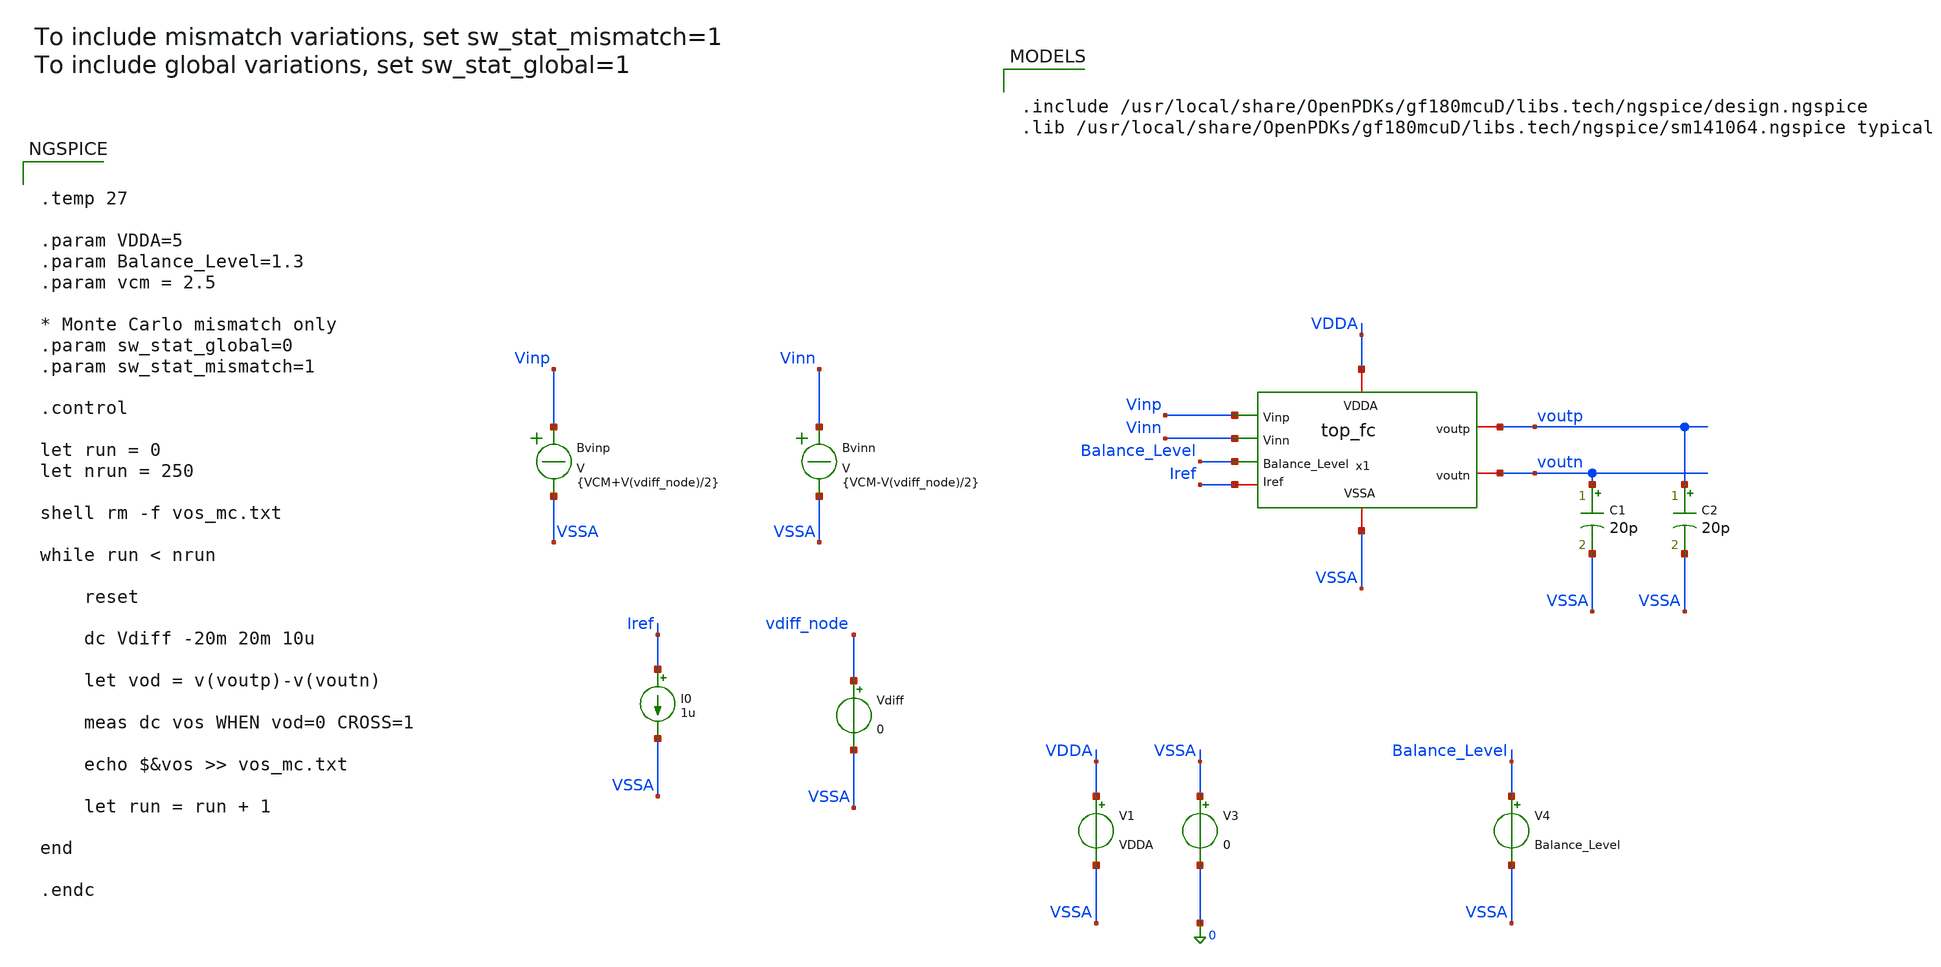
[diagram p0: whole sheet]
** sch_path: Folded_cascode/testbenches/top_fc_offset_tb.sch
**.subckt top_fc_offset_tb
Vdiff vdiff_node VSSA 0
V1 VDDA VSSA VDDA
V3 VSSA 0 0
V4 Balance_Level VSSA Balance_Level
Bvinp Vinp VSSA V = {VCM+V(vdiff_node)/2}
Bvinn Vinn VSSA V = {VCM-V(vdiff_node)/2}
x1 Balance_Level Vinp voutp VDDA voutn Vinn Iref VSSA top_fc
C1 voutn VSSA 20p m=1
C2 voutp VSSA 20p m=1
I0 Iref VSSA 1u
**** begin user architecture code

.include /usr/local/share/OpenPDKs/gf180mcuD/libs.tech/ngspice/design.ngspice
.lib /usr/local/share/OpenPDKs/gf180mcuD/libs.tech/ngspice/sm141064.ngspice typical



.temp 27

.param VDDA=5
.param Balance_Level=1.3
.param vcm = 2.5

* Monte Carlo mismatch only
.param sw_stat_global=0
.param sw_stat_mismatch=1

.control

let run = 0
let nrun = 250

shell rm -f vos_mc.txt

while run < nrun

    reset

    dc Vdiff -20m 20m 10u

    let vod = v(voutp)-v(voutn)

    meas dc vos WHEN vod=0 CROSS=1

    echo $&vos >> vos_mc.txt

    let run = run + 1

end

.endc


**** end user architecture code
**.ends
.end
